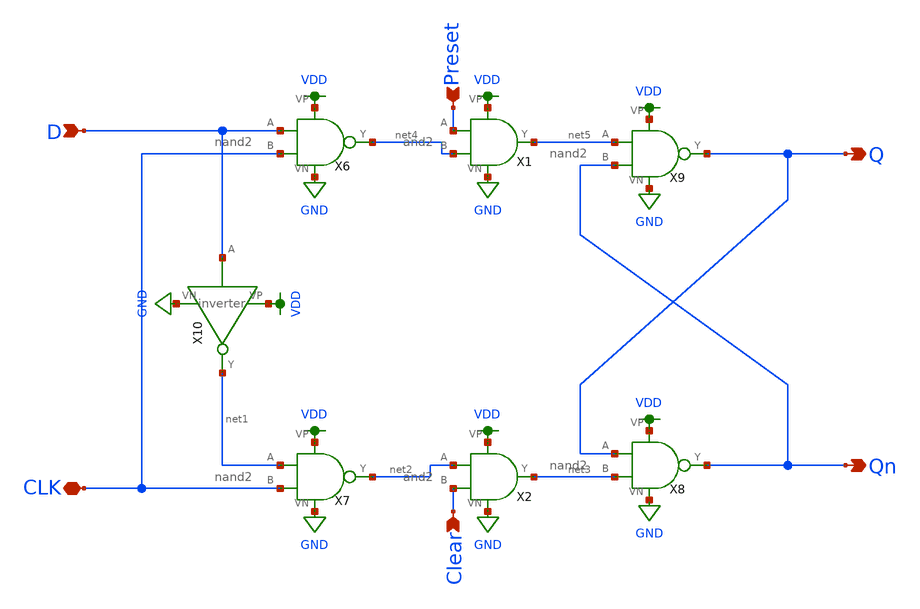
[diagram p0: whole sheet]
** sch_path: schematic/dff.sch
**.subckt dff D CLK Qn Q Preset Clear
*.ipin D
*.iopin CLK
*.opin Qn
*.opin Q
*.ipin Preset
*.ipin Clear
X6 D CLK net4 VDD GND nand2
X7 net1 CLK net2 VDD GND nand2
X8 Q net3 Qn VDD GND nand2
X9 net5 Qn Q VDD GND nand2
X10 D net1 VDD GND inverter
X1 VDD Preset GND net5 net4 and2
X2 VDD net2 GND net3 Clear and2
**.ends

* expanding   symbol:  /home/madvlsi/Documents/MADVLSI-Final_Project/schematic/nand2.sym # of pins=5
** sym_path: schematic/nand2.sym
** sch_path: schematic/nand2.sch
.subckt nand2 A B Y VP VN
*.ipin A
*.opin Y
*.ipin B
*.iopin VP
*.iopin VP
*.iopin VN
*.iopin VN
XM1 Y A VP VP sky130_fd_pr__pfet_01v8 L=0.15 W=2 nf=1 ad='int((nf+1)/2) * W/nf * 0.29' as='int((nf+2)/2) * W/nf * 0.29'
+ pd='2*int((nf+1)/2) * (W/nf + 0.29)' ps='2*int((nf+2)/2) * (W/nf + 0.29)' nrd='0.29 / W' nrs='0.29 / W'
+ sa=0 sb=0 sd=0 mult=1 m=1
XM2 VP B Y VP sky130_fd_pr__pfet_01v8 L=0.15 W=2 nf=1 ad='int((nf+1)/2) * W/nf * 0.29' as='int((nf+2)/2) * W/nf * 0.29'
+ pd='2*int((nf+1)/2) * (W/nf + 0.29)' ps='2*int((nf+2)/2) * (W/nf + 0.29)' nrd='0.29 / W' nrs='0.29 / W'
+ sa=0 sb=0 sd=0 mult=1 m=1
XM3 net1 B Y VN sky130_fd_pr__nfet_01v8 L=0.15 W=2 nf=1 ad='int((nf+1)/2) * W/nf * 0.29' as='int((nf+2)/2) * W/nf * 0.29'
+ pd='2*int((nf+1)/2) * (W/nf + 0.29)' ps='2*int((nf+2)/2) * (W/nf + 0.29)' nrd='0.29 / W' nrs='0.29 / W'
+ sa=0 sb=0 sd=0 mult=1 m=1
XM4 net1 A VN VN sky130_fd_pr__nfet_01v8 L=0.15 W=2 nf=1 ad='int((nf+1)/2) * W/nf * 0.29' as='int((nf+2)/2) * W/nf * 0.29'
+ pd='2*int((nf+1)/2) * (W/nf + 0.29)' ps='2*int((nf+2)/2) * (W/nf + 0.29)' nrd='0.29 / W' nrs='0.29 / W'
+ sa=0 sb=0 sd=0 mult=1 m=1
.ends


* expanding   symbol:  /home/madvlsi/Documents/MADVLSI-Final_Project/schematic/inverter.sym # of
*+ pins=4
** sym_path: schematic/inverter.sym
** sch_path: schematic/inverter.sch
.subckt inverter A Y VP VN
*.opin Y
*.ipin A
*.iopin VP
*.iopin VN
XM3 Y A VP VDD sky130_fd_pr__pfet_01v8 L={Lp} W={Wp} nf=1 ad='int((nf+1)/2) * W/nf * 0.29' as='int((nf+2)/2) * W/nf * 0.29'
+ pd='2*int((nf+1)/2) * (W/nf + 0.29)' ps='2*int((nf+2)/2) * (W/nf + 0.29)' nrd='0.29 / W' nrs='0.29 / W'
+ sa=0 sb=0 sd=0 mult=1 m=1
XM4 Y A VP VDD sky130_fd_pr__pfet_01v8 L={Lp} W={Wp} nf=1 ad='int((nf+1)/2) * W/nf * 0.29' as='int((nf+2)/2) * W/nf * 0.29'
+ pd='2*int((nf+1)/2) * (W/nf + 0.29)' ps='2*int((nf+2)/2) * (W/nf + 0.29)' nrd='0.29 / W' nrs='0.29 / W'
+ sa=0 sb=0 sd=0 mult=1 m=1
XM5 Y A VN GND sky130_fd_pr__nfet_01v8 L={Lp} W={Wp} nf=1 ad='int((nf+1)/2) * W/nf * 0.29' as='int((nf+2)/2) * W/nf * 0.29'
+ pd='2*int((nf+1)/2) * (W/nf + 0.29)' ps='2*int((nf+2)/2) * (W/nf + 0.29)' nrd='0.29 / W' nrs='0.29 / W'
+ sa=0 sb=0 sd=0 mult=1 m=1
.ends


* expanding   symbol:  /home/madvlsi/Documents/MADVLSI-Final_Project/schematic/and2.sym # of pins=5
** sym_path: schematic/and2.sym
** sch_path: schematic/and2.sch
.subckt and2 VP A VN Y B
*.iopin VP
*.iopin VN
*.ipin A
*.ipin B
*.opin Y
X1 A B net1 VP VN nand2
X2 net1 Y VP VN inverter
.ends

.GLOBAL VDD
.GLOBAL GND
.end
